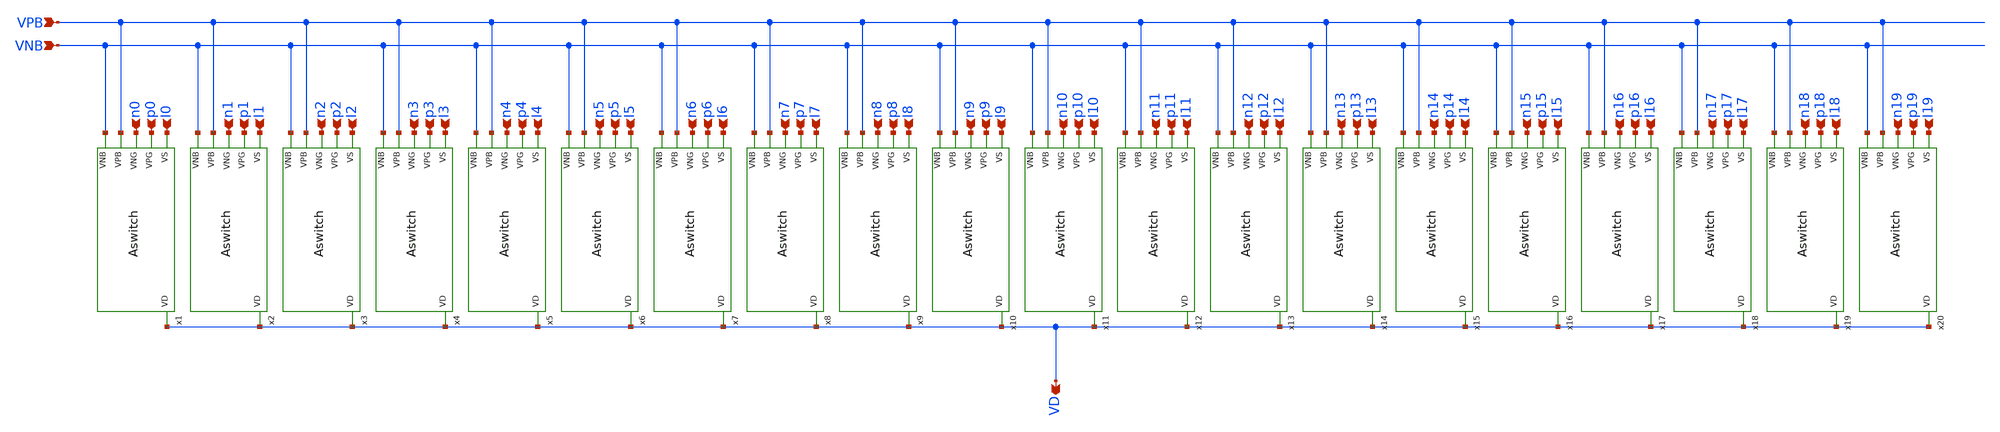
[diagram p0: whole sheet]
** sch_path: analog/schematics/switch_x20.sch
**.subckt switch_x20 VPB VNB VD n0 p0 I0 n1 p1 I1 n2 p2 I2 n3 p3 I3 n4 p4 I4 n5 p5 I5 n6 p6 I6 n7 p7
*+ I7 n8 p8 I8 n9 p9 I9 n10 p10 I10 n11 p11 I11 n12 p12 I12 n13 p13 I13 n14 p14 I14 n15 p15 I15 n16 p16
*+ I16 n17 p17 I17 n18 p18 I18 n19 p19 I19
*.ipin VPB
*.ipin VNB
*.opin VD
*.ipin n0
*.ipin p0
*.ipin I0
*.ipin n1
*.ipin p1
*.ipin I1
*.ipin n2
*.ipin p2
*.ipin I2
*.ipin n3
*.ipin p3
*.ipin I3
*.ipin n4
*.ipin p4
*.ipin I4
*.ipin n5
*.ipin p5
*.ipin I5
*.ipin n6
*.ipin p6
*.ipin I6
*.ipin n7
*.ipin p7
*.ipin I7
*.ipin n8
*.ipin p8
*.ipin I8
*.ipin n9
*.ipin p9
*.ipin I9
*.ipin n10
*.ipin p10
*.ipin I10
*.ipin n11
*.ipin p11
*.ipin I11
*.ipin n12
*.ipin p12
*.ipin I12
*.ipin n13
*.ipin p13
*.ipin I13
*.ipin n14
*.ipin p14
*.ipin I14
*.ipin n15
*.ipin p15
*.ipin I15
*.ipin n16
*.ipin p16
*.ipin I16
*.ipin n17
*.ipin p17
*.ipin I17
*.ipin n18
*.ipin p18
*.ipin I18
*.ipin n19
*.ipin p19
*.ipin I19
x1 I0 p0 n0 VPB VNB VD Aswitch
x2 I1 p1 n1 VPB VNB VD Aswitch
x3 I2 p2 n2 VPB VNB VD Aswitch
x4 I3 p3 n3 VPB VNB VD Aswitch
x5 I4 p4 n4 VPB VNB VD Aswitch
x6 I5 p5 n5 VPB VNB VD Aswitch
x7 I6 p6 n6 VPB VNB VD Aswitch
x8 I7 p7 n7 VPB VNB VD Aswitch
x9 I8 p8 n8 VPB VNB VD Aswitch
x10 I9 p9 n9 VPB VNB VD Aswitch
x11 I10 p10 n10 VPB VNB VD Aswitch
x12 I11 p11 n11 VPB VNB VD Aswitch
x13 I12 p12 n12 VPB VNB VD Aswitch
x14 I13 p13 n13 VPB VNB VD Aswitch
x15 I14 p14 n14 VPB VNB VD Aswitch
x16 I15 p15 n15 VPB VNB VD Aswitch
x17 I16 p16 n16 VPB VNB VD Aswitch
x18 I17 p17 n17 VPB VNB VD Aswitch
x19 I18 p18 n18 VPB VNB VD Aswitch
x20 I19 p19 n19 VPB VNB VD Aswitch
**.ends

* expanding   symbol:  Aswitch.sym # of pins=6
** sym_path: analog/schematics/Aswitch.sym
** sch_path: analog/schematics/Aswitch.sch
.subckt Aswitch VS VPG VNG VPB VNB VD
*.ipin VPG
*.ipin VPB
*.ipin VNB
*.ipin VNG
*.ipin VS
*.opin VD
XM1 VD VNG VS VNB sky130_fd_pr__nfet_01v8 L=0.15 W=1 nf=1 ad='int((nf+1)/2) * W/nf * 0.29' as='int((nf+2)/2) * W/nf * 0.29'
+ pd='2*int((nf+1)/2) * (W/nf + 0.29)' ps='2*int((nf+2)/2) * (W/nf + 0.29)' nrd='0.29 / W' nrs='0.29 / W'
+ sa=0 sb=0 sd=0 mult=1 m=1
XM2 VD VPG VS VPB sky130_fd_pr__pfet_01v8 L=0.15 W=1 nf=1 ad='int((nf+1)/2) * W/nf * 0.29' as='int((nf+2)/2) * W/nf * 0.29'
+ pd='2*int((nf+1)/2) * (W/nf + 0.29)' ps='2*int((nf+2)/2) * (W/nf + 0.29)' nrd='0.29 / W' nrs='0.29 / W'
+ sa=0 sb=0 sd=0 mult=1 m=1
.ends

.end
